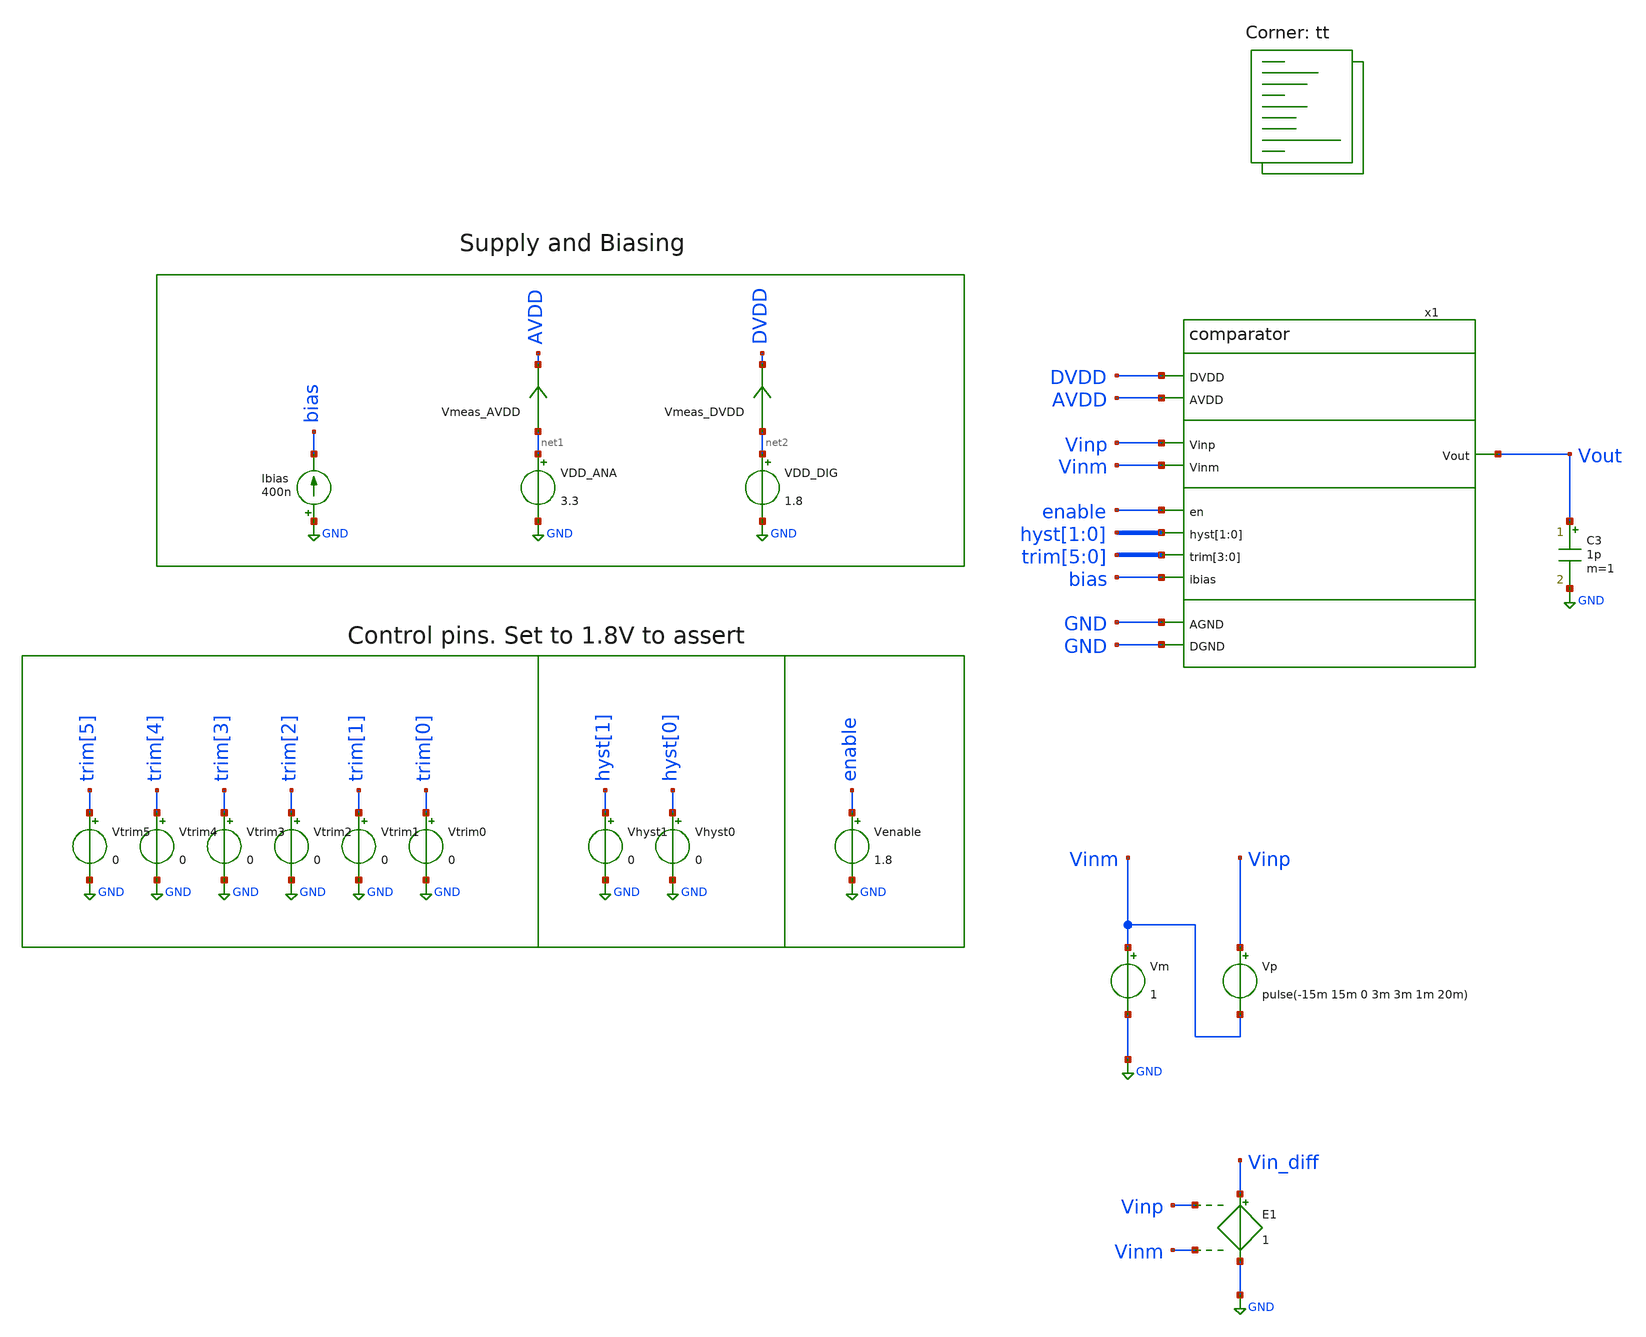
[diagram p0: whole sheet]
** sch_path: xschem/tb_comparator_trim_tran.sch
**.subckt tb_comparator_trim_tran
Vp Vinp Vinm pulse(-15m 15m 0 3m 3m 1m 20m)
VDD_ANA net1 GND 3.3
VDD_DIG net2 GND 1.8
Ibias GND bias 400n
C3 Vout GND 1p m=1
Vm Vinm GND 1
Vmeas_AVDD net1 AVDD 0
.save i(vmeas_avdd)
Vmeas_DVDD net2 DVDD 0
.save i(vmeas_dvdd)
E1 Vin_diff GND Vinp Vinm 1
Vtrim3 trim[3] GND 0
Vtrim2 trim[2] GND 0
Vtrim1 trim[1] GND 0
Vtrim0 trim[0] GND 0
Vhyst1 hyst[1] GND 0
Vhyst0 hyst[0] GND 0
Venable enable GND 1.8
Vtrim5 trim[5] GND 0
Vtrim4 trim[4] GND 0
x1 DVDD AVDD GND GND Vinp Vout Vinm enable hyst[1] hyst[0] trim[5] trim[4] trim[3] trim[2] bias
+ comparator
**** begin user architecture code
.lib $::SKYWATER_MODELS/sky130.lib.spice tt


.save v(vout) v(vin_diff)
*.save all
.tran 1u 2.5m 500u uic
.ic v(x1.vop)=0 v(x1.vdiff)=1.8 v(x1.vout_int)=0 v(x1.voutb)=1.8 v(vout)=0 v(x1.trim0_hv)=0
+  v(x1.trim1_hv)=0 v(x1.trim2_hv)=0 v(x1.trim3_hv)=0 v(x1.trim4_hv)=0 v(x1.trim5_hv)=0  v(x1.hyst1_hv)=0
+ v(x1.hyst0_hv)=0 v(x1.enb_hv)=0

.control
let num_meas = 45
let input_offset = unitvec(num_meas)
let i = 0
dowhile i<num_meas
   let input_offset[i]=0
   let i=i+1
end
let i=0
foreach temp_val -40 25 85
   foreach vdd_ana_val 2.95 3.3 5.5
      foreach vm_val 0.02 {$vdd_ana_val/4} {$vdd_ana_val/2} {$vdd_ana_val*0.75} {-0.02+$vdd_ana_val}
         foreach ibias_val 400n
            set temp=$temp_val
            alter VDD_ANA $vdd_ana_val
            alter Vm $vm_val
            alter ibias $ibias_val
            run
            print i
            echo temp: $temp_val
            echo VDDA: $vdd_ana_val
            echo Vinm: $vm_val
            echo Ibias: $ibias_val
            meas tran t_cross when v(vout)=0.9 rise=1
            meas tran in_cross find v(vin_diff) at=t_cross
            print vecmin(input_offset)
            print vecmax(input_offset)
            let input_offset[i] = in_cross
            let i = i+1
         end
      end
   end
end
set filetype = ascii
write results_trim_tt.raw input_offset
print vecmin(input_offset)
print vecmax(input_offset)
.endc


**** end user architecture code
**.ends
.GLOBAL GND
.end
